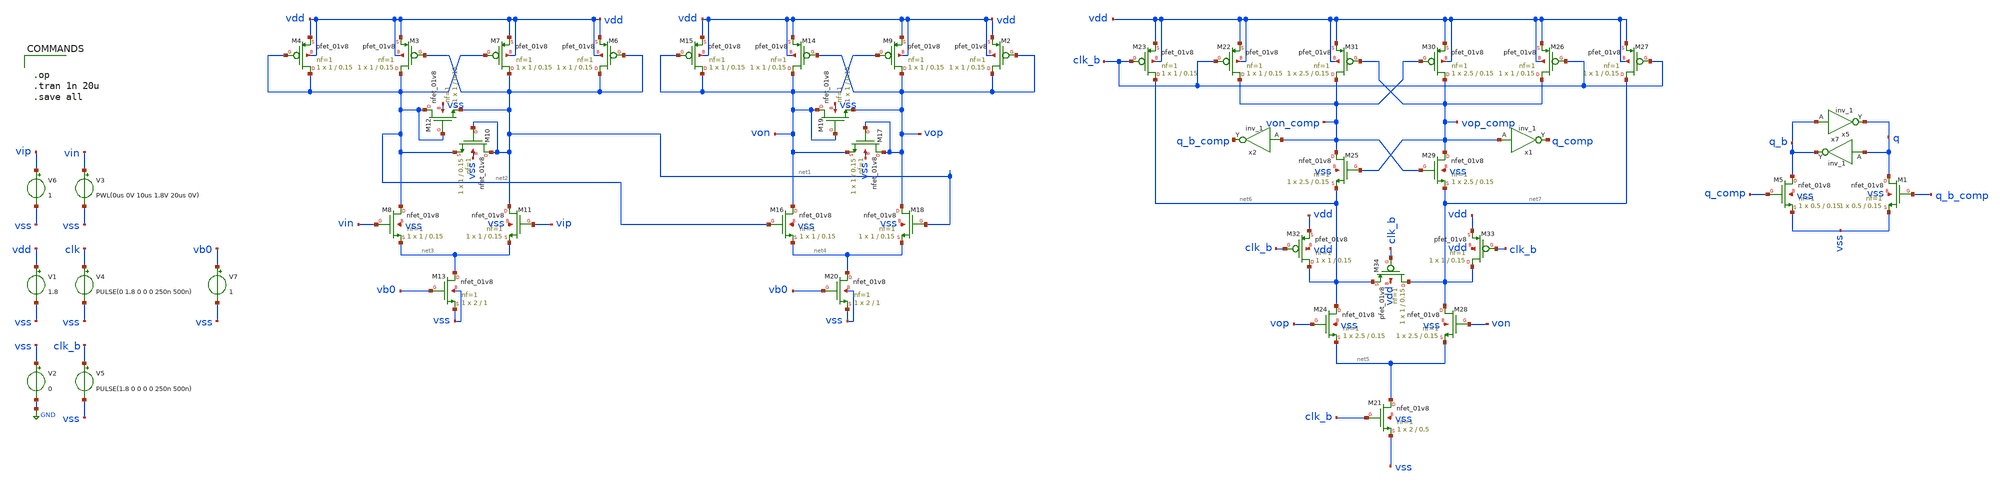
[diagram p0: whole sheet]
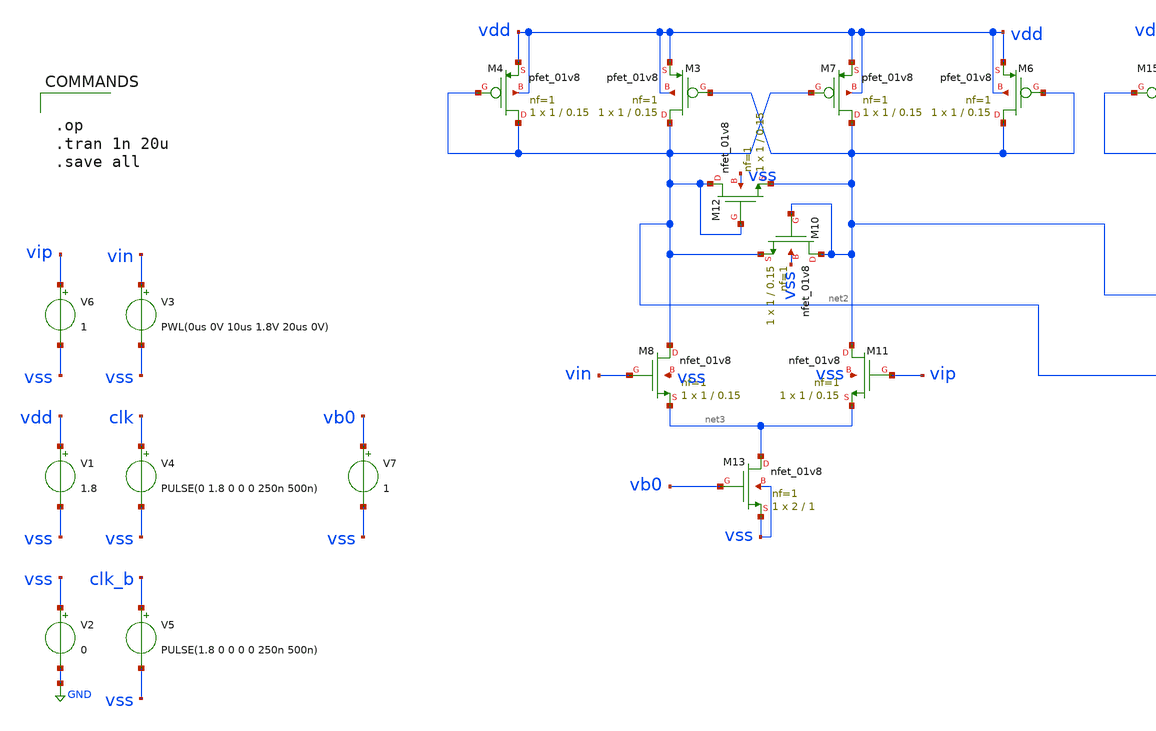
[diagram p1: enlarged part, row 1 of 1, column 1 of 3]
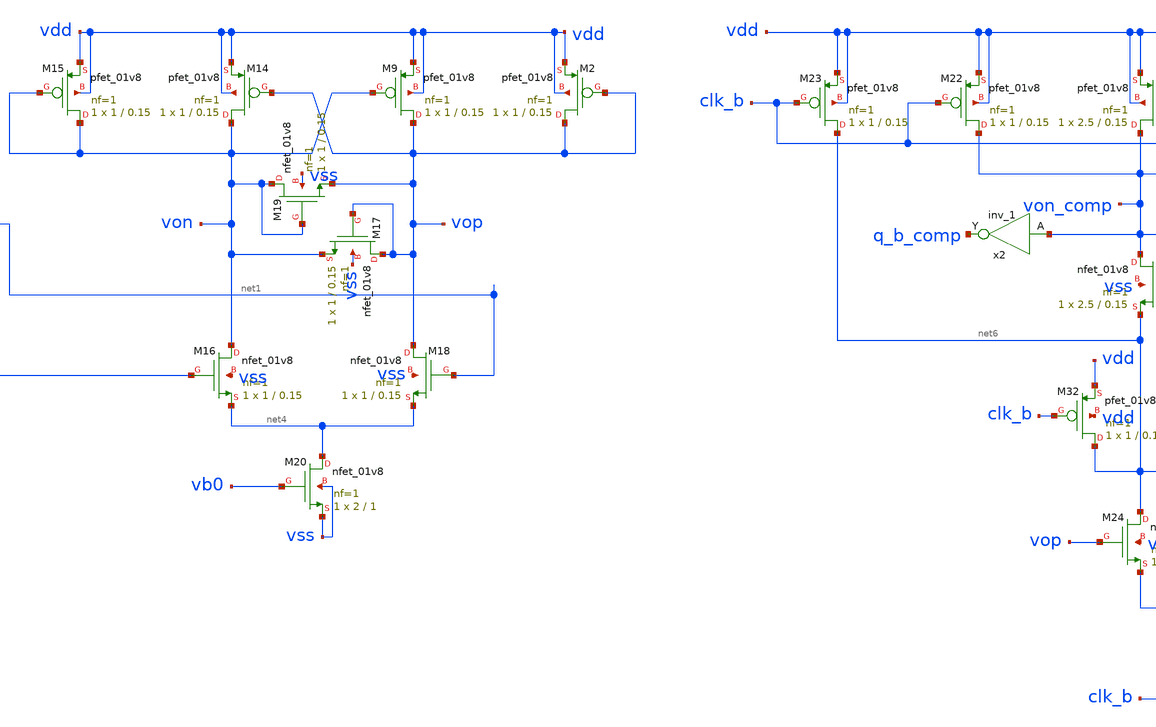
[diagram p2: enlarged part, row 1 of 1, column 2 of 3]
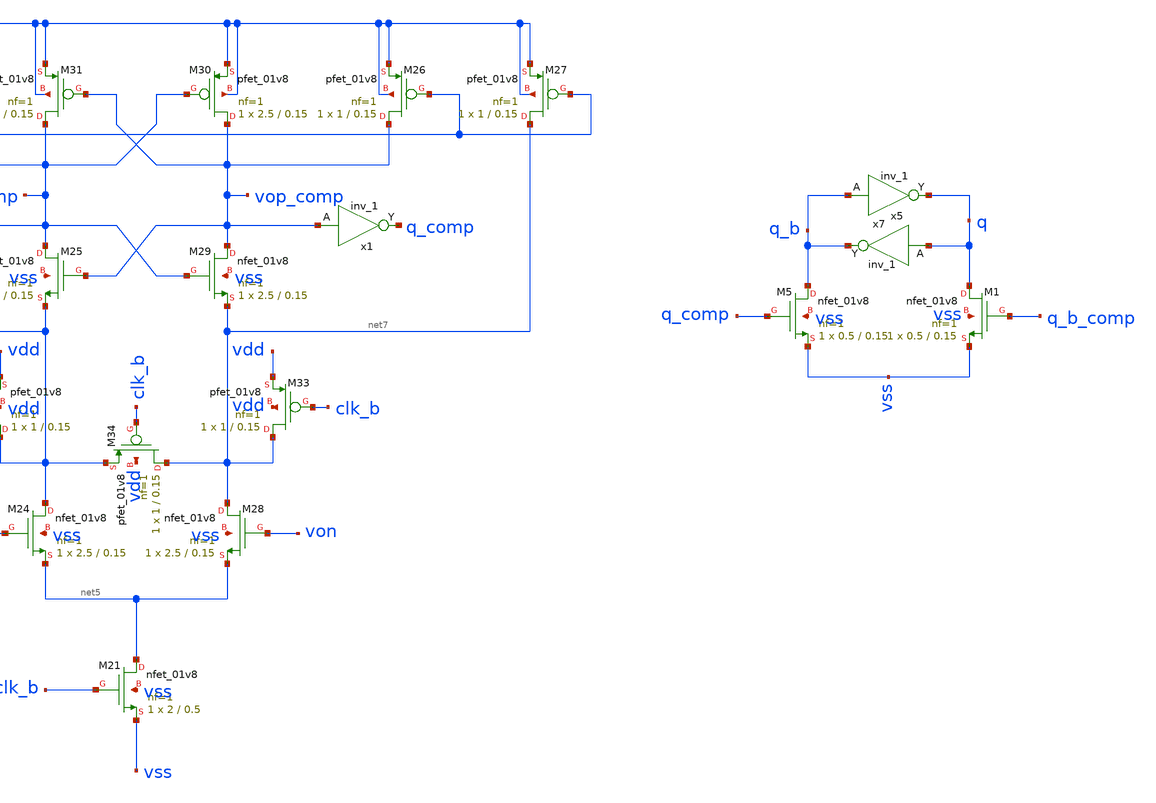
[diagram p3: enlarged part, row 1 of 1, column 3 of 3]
** sch_path: xschem/comparator/comparator_tb.sch
.lib $::SKYWATER_MODELS/sky130.lib.spice tt
.include $::SKYWATER_STDCELLS/sky130_fd_sc_hd.spice

**.subckt comparator_tb
V1 vdd vss 1.8
V3 vin vss PWL(0us 0V 10us 1.8V 20us 0V)
V4 clk vss PULSE(0 1.8 0 0 0 250n 500n)
V5 clk_b vss PULSE(1.8 0 0 0 0 250n 500n)
V6 vip vss 1
V2 vss GND 0
XM6 net1 net1 vdd vdd sky130_fd_pr__pfet_01v8 L=0.15 W=1 nf=1 ad='int((nf+1)/2) * W/nf * 0.29' as='int((nf+2)/2) * W/nf * 0.29'
+ pd='2*int((nf+1)/2) * (W/nf + 0.29)' ps='2*int((nf+2)/2) * (W/nf + 0.29)' nrd='0.29 / W' nrs='0.29 / W'
+ sa=0 sb=0 sd=0 mult=1 m=1
XM7 net1 net2 vdd vdd sky130_fd_pr__pfet_01v8 L=0.15 W=1 nf=1 ad='int((nf+1)/2) * W/nf * 0.29' as='int((nf+2)/2) * W/nf * 0.29'
+ pd='2*int((nf+1)/2) * (W/nf + 0.29)' ps='2*int((nf+2)/2) * (W/nf + 0.29)' nrd='0.29 / W' nrs='0.29 / W'
+ sa=0 sb=0 sd=0 mult=1 m=1
XM3 net2 net1 vdd vdd sky130_fd_pr__pfet_01v8 L=0.15 W=1 nf=1 ad='int((nf+1)/2) * W/nf * 0.29' as='int((nf+2)/2) * W/nf * 0.29'
+ pd='2*int((nf+1)/2) * (W/nf + 0.29)' ps='2*int((nf+2)/2) * (W/nf + 0.29)' nrd='0.29 / W' nrs='0.29 / W'
+ sa=0 sb=0 sd=0 mult=1 m=1
XM4 net2 net2 vdd vdd sky130_fd_pr__pfet_01v8 L=0.15 W=1 nf=1 ad='int((nf+1)/2) * W/nf * 0.29' as='int((nf+2)/2) * W/nf * 0.29'
+ pd='2*int((nf+1)/2) * (W/nf + 0.29)' ps='2*int((nf+2)/2) * (W/nf + 0.29)' nrd='0.29 / W' nrs='0.29 / W'
+ sa=0 sb=0 sd=0 mult=1 m=1
XM8 net2 vin net3 vss sky130_fd_pr__nfet_01v8 L=0.15 W=1 nf=1 ad='int((1 + 1)/2) * 1 / 1 * 0.29' as='int((1 + 2)/2) * 1 / 1 * 0.29'
+ pd='2*int((1 + 1)/2) * (1 / 1 + 0.29)' ps='2*int((1 + 2)/2) * (1 / 1 + 0.29)' nrd='0.29 / 1 ' nrs='0.29 / 1 '
+ sa=0 sb=0 sd=0 mult=1 m=1
XM10 net1 net1 net2 vss sky130_fd_pr__nfet_01v8 L=0.15 W=1 nf=1 ad='int((1 + 1)/2) * 1 / 1 * 0.29' as='int((1 + 2)/2) * 1 / 1 * 0.29'
+ pd='2*int((1 + 1)/2) * (1 / 1 + 0.29)' ps='2*int((1 + 2)/2) * (1 / 1 + 0.29)' nrd='0.29 / 1 ' nrs='0.29 / 1 '
+ sa=0 sb=0 sd=0 mult=1 m=1
XM11 net1 vip net3 vss sky130_fd_pr__nfet_01v8 L=0.15 W=1 nf=1 ad='int((1 + 1)/2) * 1 / 1 * 0.29' as='int((1 + 2)/2) * 1 / 1 * 0.29'
+ pd='2*int((1 + 1)/2) * (1 / 1 + 0.29)' ps='2*int((1 + 2)/2) * (1 / 1 + 0.29)' nrd='0.29 / 1 ' nrs='0.29 / 1 '
+ sa=0 sb=0 sd=0 mult=1 m=1
XM12 net2 net2 net1 vss sky130_fd_pr__nfet_01v8 L=0.15 W=1 nf=1 ad='int((1 + 1)/2) * 1 / 1 * 0.29' as='int((1 + 2)/2) * 1 / 1 * 0.29'
+ pd='2*int((1 + 1)/2) * (1 / 1 + 0.29)' ps='2*int((1 + 2)/2) * (1 / 1 + 0.29)' nrd='0.29 / 1 ' nrs='0.29 / 1 '
+ sa=0 sb=0 sd=0 mult=1 m=1
XM13 net3 vb0 vss vss sky130_fd_pr__nfet_01v8 L=1 W=2 nf=1 ad='int((1 + 1)/2) * 2 / 1 * 0.29' as='int((1 + 2)/2) * 2 / 1 * 0.29'
+ pd='2*int((1 + 1)/2) * (2 / 1 + 0.29)' ps='2*int((1 + 2)/2) * (2 / 1 + 0.29)' nrd='0.29 / 2 ' nrs='0.29 / 2 '
+ sa=0 sb=0 sd=0 mult=1 m=1
V7 vb0 vss 1
x1 vop_comp vss vss vdd vdd q_comp sky130_fd_sc_hd__inv_1
x2 von_comp vss vss vdd vdd q_b_comp sky130_fd_sc_hd__inv_1
XM5 q_b q_comp vss vss sky130_fd_pr__nfet_01v8 L=0.15 W=0.5 nf=1 ad='int((1 + 1)/2) * 0.5 / 1 * 0.29'
+ as='int((1 + 2)/2) * 0.5 / 1 * 0.29' pd='2*int((1 + 1)/2) * (0.5 / 1 + 0.29)' ps='2*int((1 + 2)/2) * (0.5 / 1 + 0.29)'
+ nrd='0.29 / 0.5 ' nrs='0.29 / 0.5 ' sa=0 sb=0 sd=0 mult=1 m=1
XM1 q q_b_comp vss vss sky130_fd_pr__nfet_01v8 L=0.15 W=0.5 nf=1 ad='int((1 + 1)/2) * 0.5 / 1 * 0.29'
+ as='int((1 + 2)/2) * 0.5 / 1 * 0.29' pd='2*int((1 + 1)/2) * (0.5 / 1 + 0.29)' ps='2*int((1 + 2)/2) * (0.5 / 1 + 0.29)'
+ nrd='0.29 / 0.5 ' nrs='0.29 / 0.5 ' sa=0 sb=0 sd=0 mult=1 m=1
x5 q_b vss vss vdd vdd q sky130_fd_sc_hd__inv_1
x7 q vss vss vdd vdd q_b sky130_fd_sc_hd__inv_1
XM2 vop vop vdd vdd sky130_fd_pr__pfet_01v8 L=0.15 W=1 nf=1 ad='int((nf+1)/2) * W/nf * 0.29' as='int((nf+2)/2) * W/nf * 0.29'
+ pd='2*int((nf+1)/2) * (W/nf + 0.29)' ps='2*int((nf+2)/2) * (W/nf + 0.29)' nrd='0.29 / W' nrs='0.29 / W'
+ sa=0 sb=0 sd=0 mult=1 m=1
XM9 vop von vdd vdd sky130_fd_pr__pfet_01v8 L=0.15 W=1 nf=1 ad='int((nf+1)/2) * W/nf * 0.29' as='int((nf+2)/2) * W/nf * 0.29'
+ pd='2*int((nf+1)/2) * (W/nf + 0.29)' ps='2*int((nf+2)/2) * (W/nf + 0.29)' nrd='0.29 / W' nrs='0.29 / W'
+ sa=0 sb=0 sd=0 mult=1 m=1
XM14 von vop vdd vdd sky130_fd_pr__pfet_01v8 L=0.15 W=1 nf=1 ad='int((nf+1)/2) * W/nf * 0.29' as='int((nf+2)/2) * W/nf * 0.29'
+ pd='2*int((nf+1)/2) * (W/nf + 0.29)' ps='2*int((nf+2)/2) * (W/nf + 0.29)' nrd='0.29 / W' nrs='0.29 / W'
+ sa=0 sb=0 sd=0 mult=1 m=1
XM15 von von vdd vdd sky130_fd_pr__pfet_01v8 L=0.15 W=1 nf=1 ad='int((nf+1)/2) * W/nf * 0.29' as='int((nf+2)/2) * W/nf * 0.29'
+ pd='2*int((nf+1)/2) * (W/nf + 0.29)' ps='2*int((nf+2)/2) * (W/nf + 0.29)' nrd='0.29 / W' nrs='0.29 / W'
+ sa=0 sb=0 sd=0 mult=1 m=1
XM16 von net2 net4 vss sky130_fd_pr__nfet_01v8 L=0.15 W=1 nf=1 ad='int((1 + 1)/2) * 1 / 1 * 0.29' as='int((1 + 2)/2) * 1 / 1 * 0.29'
+ pd='2*int((1 + 1)/2) * (1 / 1 + 0.29)' ps='2*int((1 + 2)/2) * (1 / 1 + 0.29)' nrd='0.29 / 1 ' nrs='0.29 / 1 '
+ sa=0 sb=0 sd=0 mult=1 m=1
XM17 vop vop von vss sky130_fd_pr__nfet_01v8 L=0.15 W=1 nf=1 ad='int((1 + 1)/2) * 1 / 1 * 0.29' as='int((1 + 2)/2) * 1 / 1 * 0.29'
+ pd='2*int((1 + 1)/2) * (1 / 1 + 0.29)' ps='2*int((1 + 2)/2) * (1 / 1 + 0.29)' nrd='0.29 / 1 ' nrs='0.29 / 1 '
+ sa=0 sb=0 sd=0 mult=1 m=1
XM18 vop net1 net4 vss sky130_fd_pr__nfet_01v8 L=0.15 W=1 nf=1 ad='int((1 + 1)/2) * 1 / 1 * 0.29' as='int((1 + 2)/2) * 1 / 1 * 0.29'
+ pd='2*int((1 + 1)/2) * (1 / 1 + 0.29)' ps='2*int((1 + 2)/2) * (1 / 1 + 0.29)' nrd='0.29 / 1 ' nrs='0.29 / 1 '
+ sa=0 sb=0 sd=0 mult=1 m=1
XM19 von von vop vss sky130_fd_pr__nfet_01v8 L=0.15 W=1 nf=1 ad='int((1 + 1)/2) * 1 / 1 * 0.29' as='int((1 + 2)/2) * 1 / 1 * 0.29'
+ pd='2*int((1 + 1)/2) * (1 / 1 + 0.29)' ps='2*int((1 + 2)/2) * (1 / 1 + 0.29)' nrd='0.29 / 1 ' nrs='0.29 / 1 '
+ sa=0 sb=0 sd=0 mult=1 m=1
XM20 net4 vb0 vss vss sky130_fd_pr__nfet_01v8 L=1 W=2 nf=1 ad='int((1 + 1)/2) * 2 / 1 * 0.29' as='int((1 + 2)/2) * 2 / 1 * 0.29'
+ pd='2*int((1 + 1)/2) * (2 / 1 + 0.29)' ps='2*int((1 + 2)/2) * (2 / 1 + 0.29)' nrd='0.29 / 2 ' nrs='0.29 / 2 '
+ sa=0 sb=0 sd=0 mult=1 m=1
XM21 net5 clk_b vss vss sky130_fd_pr__nfet_01v8 L=0.5 W=2 nf=1 ad='int((nf+1)/2) * W/nf * 0.29' as='int((nf+2)/2) * W/nf * 0.29'
+ pd='2*int((nf+1)/2) * (W/nf + 0.29)' ps='2*int((nf+2)/2) * (W/nf + 0.29)' nrd='0.29 / W' nrs='0.29 / W'
+ sa=0 sb=0 sd=0 mult=1 m=1
XM22 von_comp clk_b vdd vdd sky130_fd_pr__pfet_01v8 L=0.15 W=1 nf=1 ad='int((nf+1)/2) * W/nf * 0.29'
+ as='int((nf+2)/2) * W/nf * 0.29' pd='2*int((nf+1)/2) * (W/nf + 0.29)' ps='2*int((nf+2)/2) * (W/nf + 0.29)'
+ nrd='0.29 / W' nrs='0.29 / W' sa=0 sb=0 sd=0 mult=1 m=1
XM23 net6 clk_b vdd vdd sky130_fd_pr__pfet_01v8 L=0.15 W=1 nf=1 ad='int((nf+1)/2) * W/nf * 0.29' as='int((nf+2)/2) * W/nf * 0.29'
+ pd='2*int((nf+1)/2) * (W/nf + 0.29)' ps='2*int((nf+2)/2) * (W/nf + 0.29)' nrd='0.29 / W' nrs='0.29 / W'
+ sa=0 sb=0 sd=0 mult=1 m=1
XM24 net6 vop net5 vss sky130_fd_pr__nfet_01v8 L=0.15 W=2.5 nf=1 ad='int((nf+1)/2) * W/nf * 0.29' as='int((nf+2)/2) * W/nf * 0.29'
+ pd='2*int((nf+1)/2) * (W/nf + 0.29)' ps='2*int((nf+2)/2) * (W/nf + 0.29)' nrd='0.29 / W' nrs='0.29 / W'
+ sa=0 sb=0 sd=0 mult=1 m=1
XM25 von_comp vop_comp net6 vss sky130_fd_pr__nfet_01v8 L=0.15 W=2.5 nf=1 ad='int((nf+1)/2) * W/nf * 0.29'
+ as='int((nf+2)/2) * W/nf * 0.29' pd='2*int((nf+1)/2) * (W/nf + 0.29)' ps='2*int((nf+2)/2) * (W/nf + 0.29)'
+ nrd='0.29 / W' nrs='0.29 / W' sa=0 sb=0 sd=0 mult=1 m=1
XM26 vop_comp clk_b vdd vdd sky130_fd_pr__pfet_01v8 L=0.15 W=1 nf=1 ad='int((nf+1)/2) * W/nf * 0.29'
+ as='int((nf+2)/2) * W/nf * 0.29' pd='2*int((nf+1)/2) * (W/nf + 0.29)' ps='2*int((nf+2)/2) * (W/nf + 0.29)'
+ nrd='0.29 / W' nrs='0.29 / W' sa=0 sb=0 sd=0 mult=1 m=1
XM27 net7 clk_b vdd vdd sky130_fd_pr__pfet_01v8 L=0.15 W=1 nf=1 ad='int((nf+1)/2) * W/nf * 0.29' as='int((nf+2)/2) * W/nf * 0.29'
+ pd='2*int((nf+1)/2) * (W/nf + 0.29)' ps='2*int((nf+2)/2) * (W/nf + 0.29)' nrd='0.29 / W' nrs='0.29 / W'
+ sa=0 sb=0 sd=0 mult=1 m=1
XM28 net7 von net5 vss sky130_fd_pr__nfet_01v8 L=0.15 W=2.5 nf=1 ad='int((nf+1)/2) * W/nf * 0.29' as='int((nf+2)/2) * W/nf * 0.29'
+ pd='2*int((nf+1)/2) * (W/nf + 0.29)' ps='2*int((nf+2)/2) * (W/nf + 0.29)' nrd='0.29 / W' nrs='0.29 / W'
+ sa=0 sb=0 sd=0 mult=1 m=1
XM29 vop_comp von_comp net7 vss sky130_fd_pr__nfet_01v8 L=0.15 W=2.5 nf=1 ad='int((nf+1)/2) * W/nf * 0.29'
+ as='int((nf+2)/2) * W/nf * 0.29' pd='2*int((nf+1)/2) * (W/nf + 0.29)' ps='2*int((nf+2)/2) * (W/nf + 0.29)'
+ nrd='0.29 / W' nrs='0.29 / W' sa=0 sb=0 sd=0 mult=1 m=1
XM30 vop_comp von_comp vdd vdd sky130_fd_pr__pfet_01v8 L=0.15 W=2.5 nf=1 ad='int((nf+1)/2) * W/nf * 0.29'
+ as='int((nf+2)/2) * W/nf * 0.29' pd='2*int((nf+1)/2) * (W/nf + 0.29)' ps='2*int((nf+2)/2) * (W/nf + 0.29)'
+ nrd='0.29 / W' nrs='0.29 / W' sa=0 sb=0 sd=0 mult=1 m=1
XM31 von_comp vop_comp vdd vdd sky130_fd_pr__pfet_01v8 L=0.15 W=2.5 nf=1 ad='int((nf+1)/2) * W/nf * 0.29'
+ as='int((nf+2)/2) * W/nf * 0.29' pd='2*int((nf+1)/2) * (W/nf + 0.29)' ps='2*int((nf+2)/2) * (W/nf + 0.29)'
+ nrd='0.29 / W' nrs='0.29 / W' sa=0 sb=0 sd=0 mult=1 m=1
XM32 net6 clk_b vdd vdd sky130_fd_pr__pfet_01v8 L=0.15 W=1 nf=1 ad='int((nf+1)/2) * W/nf * 0.29' as='int((nf+2)/2) * W/nf * 0.29'
+ pd='2*int((nf+1)/2) * (W/nf + 0.29)' ps='2*int((nf+2)/2) * (W/nf + 0.29)' nrd='0.29 / W' nrs='0.29 / W'
+ sa=0 sb=0 sd=0 mult=1 m=1
XM33 net7 clk_b vdd vdd sky130_fd_pr__pfet_01v8 L=0.15 W=1 nf=1 ad='int((nf+1)/2) * W/nf * 0.29' as='int((nf+2)/2) * W/nf * 0.29'
+ pd='2*int((nf+1)/2) * (W/nf + 0.29)' ps='2*int((nf+2)/2) * (W/nf + 0.29)' nrd='0.29 / W' nrs='0.29 / W'
+ sa=0 sb=0 sd=0 mult=1 m=1
XM34 net7 clk_b net6 vdd sky130_fd_pr__pfet_01v8 L=0.15 W=1 nf=1 ad='int((nf+1)/2) * W/nf * 0.29' as='int((nf+2)/2) * W/nf * 0.29'
+ pd='2*int((nf+1)/2) * (W/nf + 0.29)' ps='2*int((nf+2)/2) * (W/nf + 0.29)' nrd='0.29 / W' nrs='0.29 / W'
+ sa=0 sb=0 sd=0 mult=1 m=1
**** begin user architecture code


.op
.tran 1n 20u
.save all


**** end user architecture code
**.ends
.GLOBAL GND
.end
